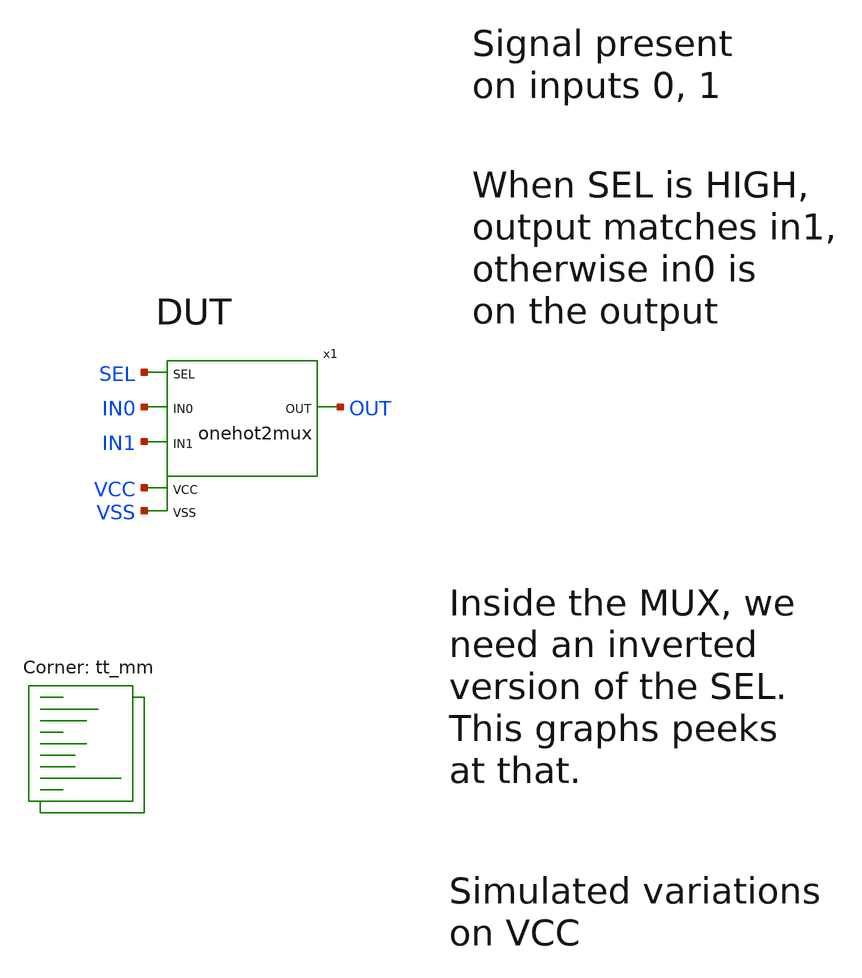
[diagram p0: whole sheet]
** sch_path: xschem/tb_onehot2mux.sch
**.subckt tb_onehot2mux
x1 VCC VSS SEL IN1 OUT IN0 onehot2mux
**** begin user architecture code
.lib $::SKYWATER_MODELS/sky130.lib.spice tt_mm


** this experimental option enables mos model bin
** selection based on W/NF instead of W
.option chgtol=4e-16 method=gear

.param VCCGAUSS = agauss(1.8, 0.05, 1)
.param VCC = 'VCCGAUSS'
** use following line to remove VCC variations
* .param VCC = 1.8
.param VDLGAUSS = agauss(0.9, 0.23, 1)
.param VDL = VDLGAUSS
** use following line to remove input common mode variations
* .param VDL =  0.9
.param TEMPGAUSS = agauss(40, 30, 1)
.option temp = 'TEMPGAUSS'
** use following line to remove temperature variations
* .option temp = 25
.param DELTA = 0.002

.include stimuli_tb_onehot2mux.cir

.control
  setseed  8
  reset
  let run = 1
  save all
  op
  write tb_onehot2mux.raw
  reset
  set appendwrite
  dowhile run < = 50
    save all
    tran 1n 1000n uic
    write tb_onehot2mux.raw
    let run = run + 1
    reset
  end
  quit 0
.endc


**** end user architecture code
**.ends
.end
